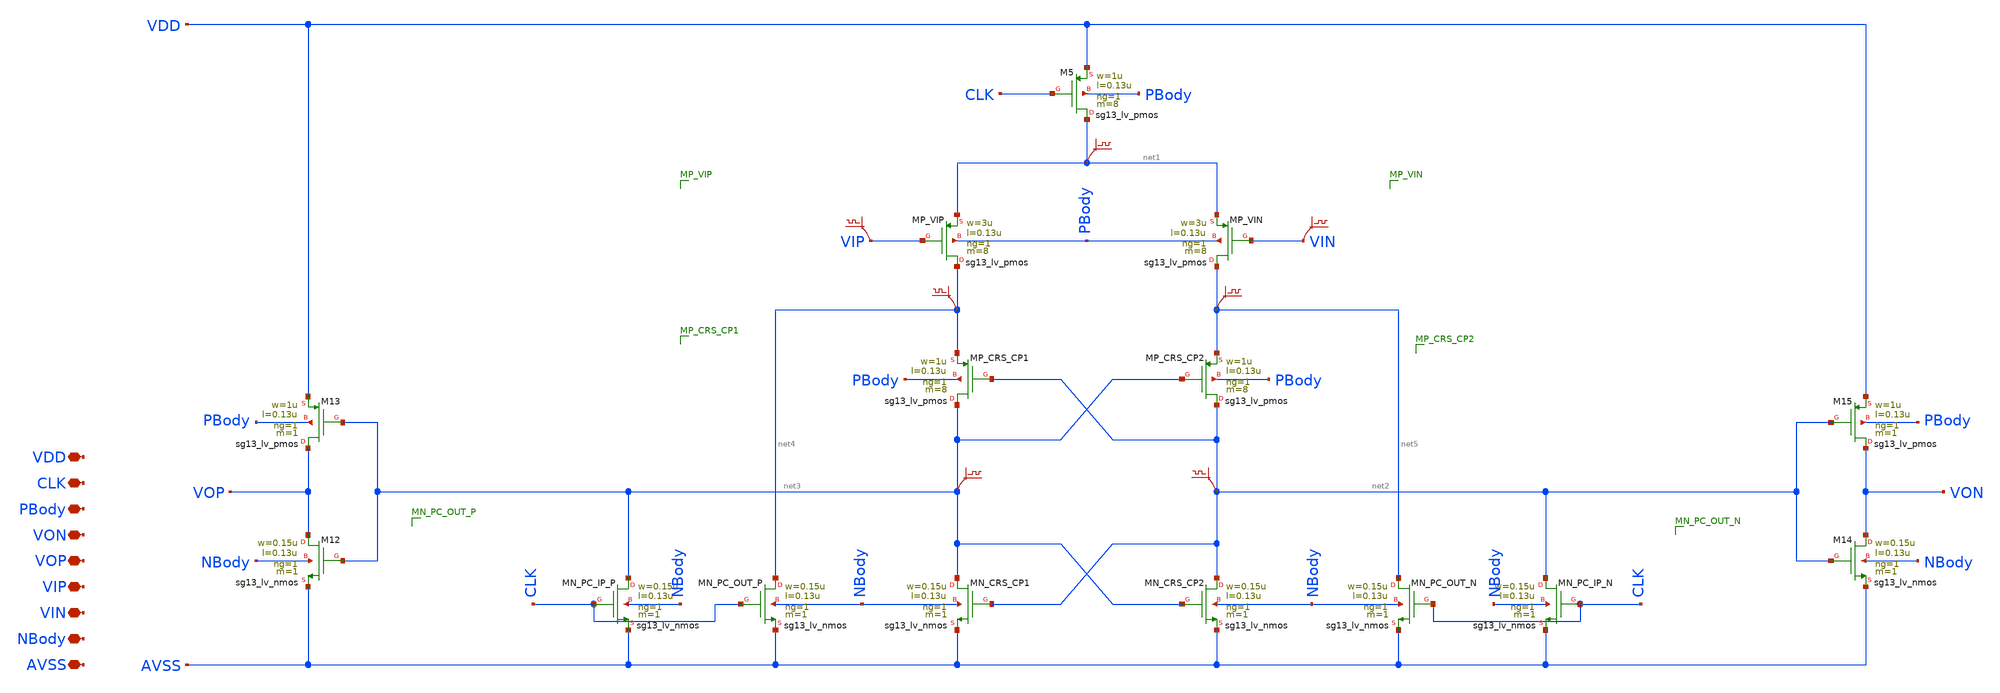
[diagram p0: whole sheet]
** sch_path: COMP/COMP_PMOS_IP.sch
**.subckt COMP_PMOS_IP VDD CLK PBody VON VOP VIP VIN NBody AVSS
*.iopin VDD
*.iopin CLK
*.iopin PBody
*.iopin VON
*.iopin VOP
*.iopin VIP
*.iopin VIN
*.iopin NBody
*.iopin AVSS
XMP_VIP net4 VIP net1 PBody sg13_lv_pmos w=3u l=0.13u ng=1 m=8 mm_ok=1
XMP_VIN net5 VIN net1 PBody sg13_lv_pmos w=3u l=0.13u ng=1 m=8 mm_ok=1
XMP_CRS_CP1 net3 net2 net4 PBody sg13_lv_pmos w=1u l=0.13u ng=1 m=8 mm_ok=1
XMP_CRS_CP2 net2 net3 net5 PBody sg13_lv_pmos w=1u l=0.13u ng=1 m=8 mm_ok=1
XM5 net1 CLK VDD PBody sg13_lv_pmos w=1u l=0.13u ng=1 m=8 mm_ok=1
XMN_CRS_CP2 net2 net3 AVSS NBody sg13_lv_nmos w=0.15u l=0.13u ng=1 m=1 mm_ok=1
XMN_CRS_CP1 net3 net2 AVSS NBody sg13_lv_nmos w=0.15u l=0.13u ng=1 m=1 mm_ok=1
XMN_PC_OUT_P net4 CLK AVSS NBody sg13_lv_nmos w=0.15u l=0.13u ng=1 m=1 mm_ok=1
XMN_PC_OUT_N net5 CLK AVSS NBody sg13_lv_nmos w=0.15u l=0.13u ng=1 m=1 mm_ok=1
XMN_PC_IP_P net3 CLK AVSS NBody sg13_lv_nmos w=0.15u l=0.13u ng=1 m=1 mm_ok=1
XMN_PC_IP_N net2 CLK AVSS NBody sg13_lv_nmos w=0.15u l=0.13u ng=1 m=1 mm_ok=1
.save v(vip)
.save v(vin)
XM12 VOP net3 AVSS NBody sg13_lv_nmos w=0.15u l=0.13u ng=1 m=1 mm_ok=1
XM13 VOP net3 VDD PBody sg13_lv_pmos w=1u l=0.13u ng=1 m=1 mm_ok=1
XM14 VON net2 AVSS NBody sg13_lv_nmos w=0.15u l=0.13u ng=1 m=1 mm_ok=1
XM15 VON net2 VDD PBody sg13_lv_pmos w=1u l=0.13u ng=1 m=1 mm_ok=1
.save v(net1)
.save v(net5)
.save v(net4)
.save v(net3)
.save v(net2)
**.ends
.end
